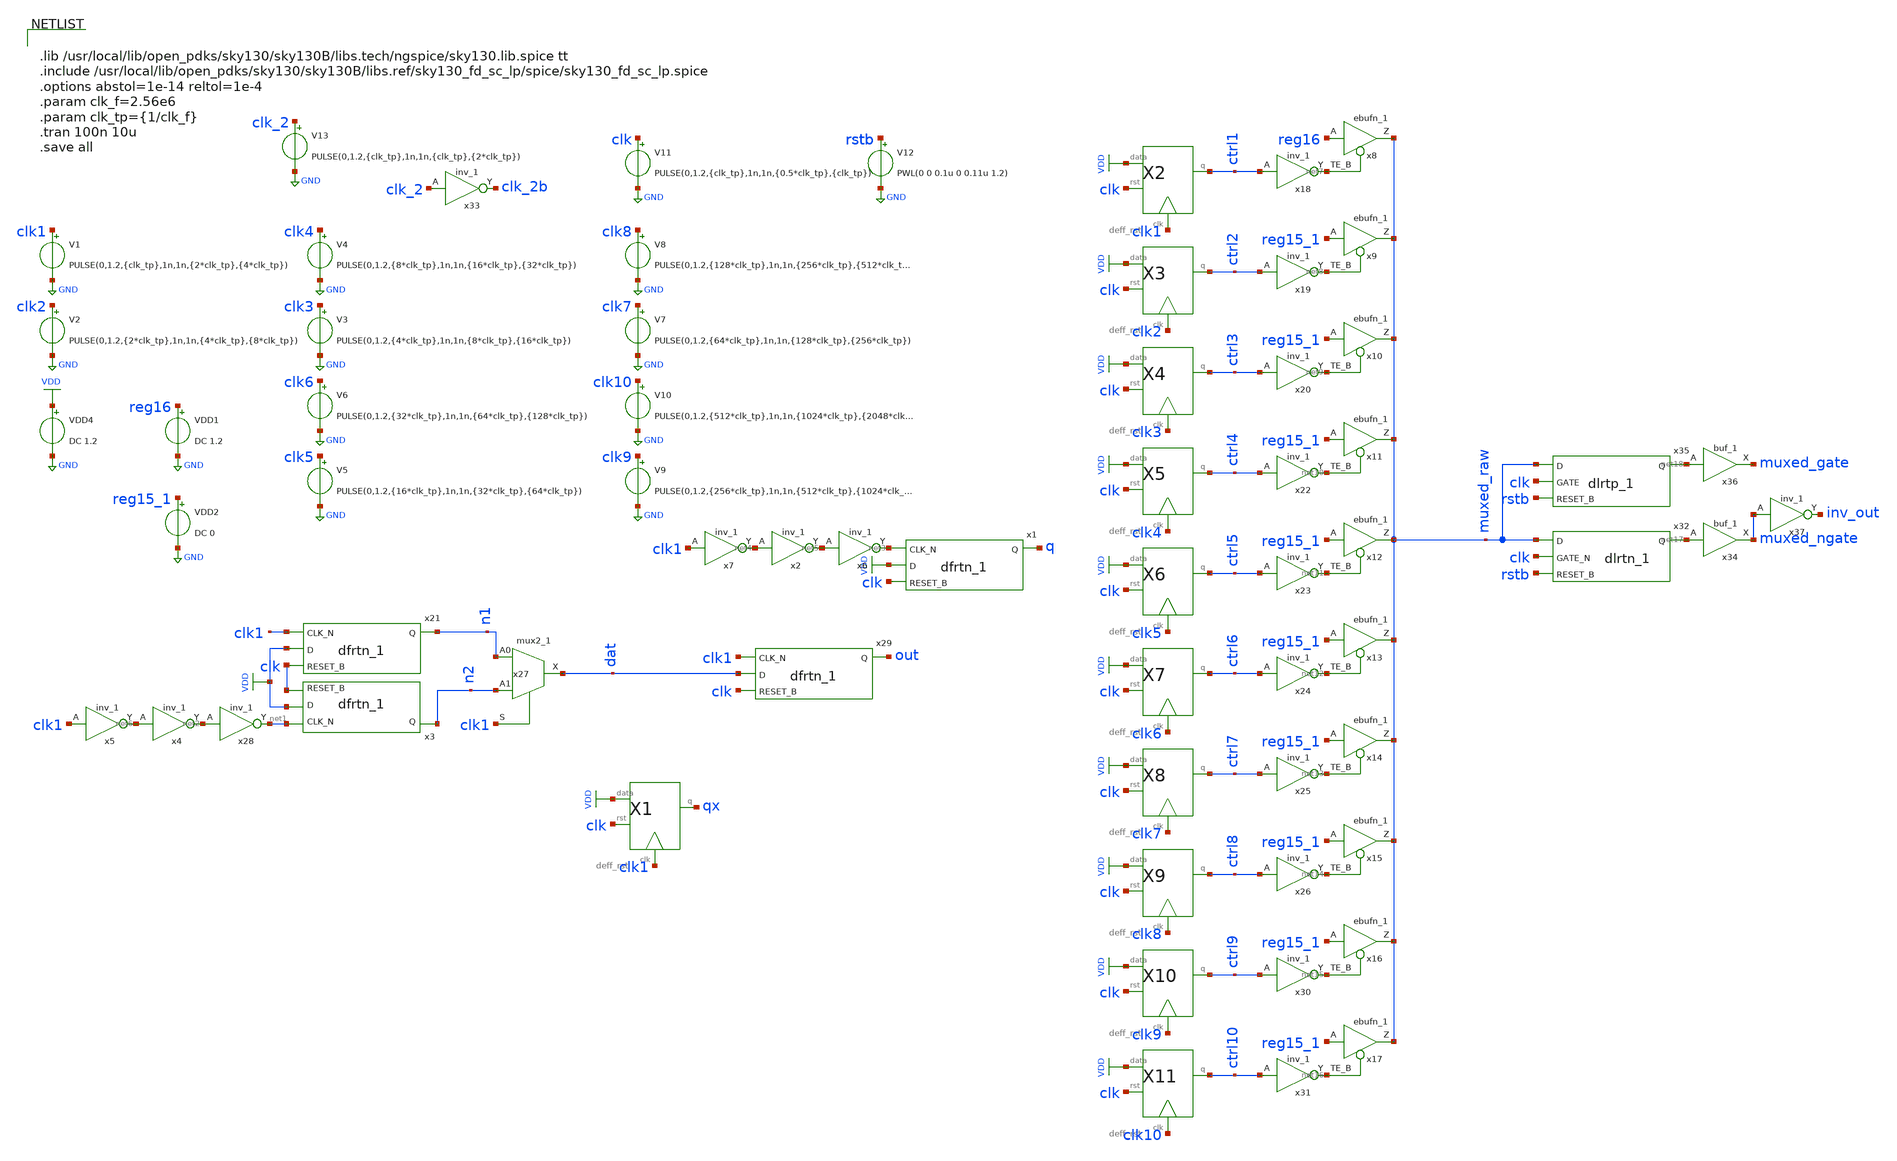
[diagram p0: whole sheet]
** sch_path: xschem/tryandtest/grayselection.sch
**.subckt grayselection
V1 clk1 GND PULSE(0,1.2,{clk_tp},1n,1n,{2*clk_tp},{4*clk_tp})
VDD4 VDD GND DC 1.2
V2 clk2 GND PULSE(0,1.2,{2*clk_tp},1n,1n,{4*clk_tp},{8*clk_tp})
V3 clk3 GND PULSE(0,1.2,{4*clk_tp},1n,1n,{8*clk_tp},{16*clk_tp})
V4 clk4 GND PULSE(0,1.2,{8*clk_tp},1n,1n,{16*clk_tp},{32*clk_tp})
V5 clk5 GND PULSE(0,1.2,{16*clk_tp},1n,1n,{32*clk_tp},{64*clk_tp})
V6 clk6 GND PULSE(0,1.2,{32*clk_tp},1n,1n,{64*clk_tp},{128*clk_tp})
V7 clk7 GND PULSE(0,1.2,{64*clk_tp},1n,1n,{128*clk_tp},{256*clk_tp})
V8 clk8 GND PULSE(0,1.2,{128*clk_tp},1n,1n,{256*clk_tp},{512*clk_tp})
V9 clk9 GND PULSE(0,1.2,{256*clk_tp},1n,1n,{512*clk_tp},{1024*clk_tp})
V10 clk10 GND PULSE(0,1.2,{512*clk_tp},1n,1n,{1024*clk_tp},{2048*clk_tp})
VDD1 reg16 GND DC 1.2
VDD2 reg15_1 GND DC 0
V11 clk GND PULSE(0,1.2,{clk_tp},1n,1n,{0.5*clk_tp},{clk_tp})
x27 n1 n2 clk1 GND GND VDD VDD dat sky130_fd_sc_lp__mux2_1
x28 net2 GND GND VDD VDD net1 sky130_fd_sc_lp__inv_1
x29 clk1 dat clk GND GND VDD VDD out sky130_fd_sc_lp__dfrtn_1
x21 clk1 VDD clk GND GND VDD VDD n1 sky130_fd_sc_lp__dfrtn_1
x1 net3 VDD clk GND GND VDD VDD q sky130_fd_sc_lp__dfrtn_1
x2 net4 GND GND VDD VDD net5 sky130_fd_sc_lp__inv_1
x6 net5 GND GND VDD VDD net3 sky130_fd_sc_lp__inv_1
x7 clk1 GND GND VDD VDD net4 sky130_fd_sc_lp__inv_1
x3 net1 VDD clk GND GND VDD VDD n2 sky130_fd_sc_lp__dfrtn_1
x4 net6 GND GND VDD VDD net2 sky130_fd_sc_lp__inv_1
x5 clk1 GND GND VDD VDD net6 sky130_fd_sc_lp__inv_1
X1 VDD clk1 qx clk deff_rst
X2 VDD clk1 ctrl1 clk deff_rst
X3 VDD clk2 ctrl2 clk deff_rst
X4 VDD clk3 ctrl3 clk deff_rst
X5 VDD clk4 ctrl4 clk deff_rst
X6 VDD clk5 ctrl5 clk deff_rst
X7 VDD clk6 ctrl6 clk deff_rst
X8 VDD clk7 ctrl7 clk deff_rst
X9 VDD clk8 ctrl8 clk deff_rst
X10 VDD clk9 ctrl9 clk deff_rst
X11 VDD clk10 ctrl10 clk deff_rst
x8 reg16 net7 GND GND VDD VDD muxed_raw sky130_fd_sc_lp__ebufn_1
x9 reg15_1 net8 GND GND VDD VDD muxed_raw sky130_fd_sc_lp__ebufn_1
x10 reg15_1 net9 GND GND VDD VDD muxed_raw sky130_fd_sc_lp__ebufn_1
x11 reg15_1 net10 GND GND VDD VDD muxed_raw sky130_fd_sc_lp__ebufn_1
x12 reg15_1 net11 GND GND VDD VDD muxed_raw sky130_fd_sc_lp__ebufn_1
x13 reg15_1 net12 GND GND VDD VDD muxed_raw sky130_fd_sc_lp__ebufn_1
x14 reg15_1 net13 GND GND VDD VDD muxed_raw sky130_fd_sc_lp__ebufn_1
x15 reg15_1 net14 GND GND VDD VDD muxed_raw sky130_fd_sc_lp__ebufn_1
x16 reg15_1 net15 GND GND VDD VDD muxed_raw sky130_fd_sc_lp__ebufn_1
x17 reg15_1 net16 GND GND VDD VDD muxed_raw sky130_fd_sc_lp__ebufn_1
x18 ctrl1 GND GND VDD VDD net7 sky130_fd_sc_lp__inv_1
x19 ctrl2 GND GND VDD VDD net8 sky130_fd_sc_lp__inv_1
x20 ctrl3 GND GND VDD VDD net9 sky130_fd_sc_lp__inv_1
x22 ctrl4 GND GND VDD VDD net10 sky130_fd_sc_lp__inv_1
x23 ctrl5 GND GND VDD VDD net11 sky130_fd_sc_lp__inv_1
x24 ctrl6 GND GND VDD VDD net12 sky130_fd_sc_lp__inv_1
x25 ctrl7 GND GND VDD VDD net13 sky130_fd_sc_lp__inv_1
x26 ctrl8 GND GND VDD VDD net14 sky130_fd_sc_lp__inv_1
x30 ctrl9 GND GND VDD VDD net15 sky130_fd_sc_lp__inv_1
x31 ctrl10 GND GND VDD VDD net16 sky130_fd_sc_lp__inv_1
V12 rstb GND PWL(0 0 0.1u 0 0.11u 1.2)
V13 clk_2 GND PULSE(0,1.2,{clk_tp},1n,1n,{clk_tp},{2*clk_tp})
x33 clk_2 GND GND VDD VDD clk_2b sky130_fd_sc_lp__inv_1
x34 net17 GND GND VDD VDD muxed_ngate sky130_fd_sc_lp__buf_1
x32 muxed_raw clk rstb GND GND VDD VDD net17 sky130_fd_sc_lp__dlrtn_1
x35 muxed_raw clk rstb GND GND VDD VDD net18 sky130_fd_sc_lp__dlrtp_1
x36 net18 GND GND VDD VDD muxed_gate sky130_fd_sc_lp__buf_1
x37 muxed_ngate GND GND VDD VDD inv_out sky130_fd_sc_lp__inv_1
**** begin user architecture code


.lib /usr/local/lib/open_pdks/sky130/sky130B/libs.tech/ngspice/sky130.lib.spice tt
.include /usr/local/lib/open_pdks/sky130/sky130B/libs.ref/sky130_fd_sc_lp/spice/sky130_fd_sc_lp.spice
.options abstol=1e-14 reltol=1e-4
.param clk_f=2.56e6
.param clk_tp={1/clk_f}
.tran 100n 10u
.save all


**** end user architecture code
**.ends

* expanding   symbol:  tryandtest/deff_rst.sym # of pins=4
** sym_path: xschem/tryandtest/deff_rst.sym
** sch_path: xschem/tryandtest/deff_rst.sch
.subckt deff_rst data clk q rst
*.ipin clk
*.ipin data
*.opin q
*.ipin rst
x3 net2 net3 clk GND GND VDD VDD q sky130_fd_sc_lp__mux2_1
x21 net1 data rst GND GND VDD VDD net2 sky130_fd_sc_lp__dfrtn_1
x2 net4 GND GND VDD VDD net1 sky130_fd_sc_lp__inv_1
x5 net5 GND GND VDD VDD net4 sky130_fd_sc_lp__inv_1
x1 net1 data rst GND GND VDD VDD net3 sky130_fd_sc_lp__dfrtp_1
x4 net6 GND GND VDD VDD net5 sky130_fd_sc_lp__inv_1
x6 clk GND GND VDD VDD net6 sky130_fd_sc_lp__inv_1
.ends

.GLOBAL GND
.GLOBAL VDD
.end
